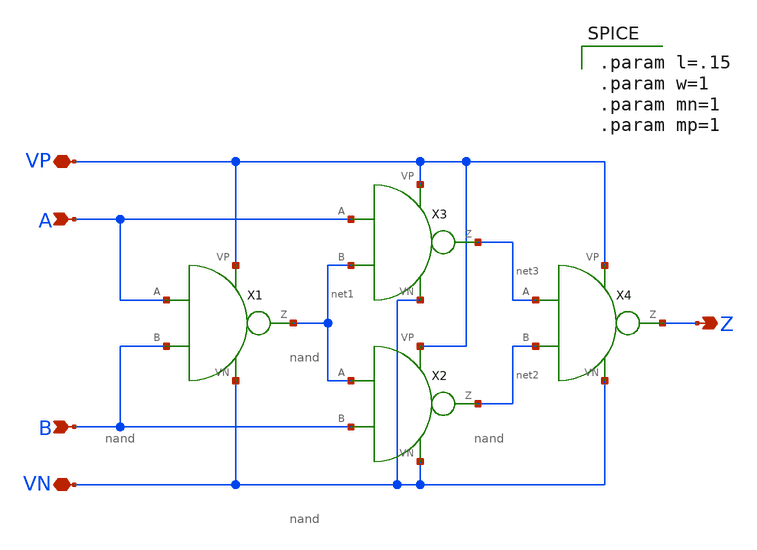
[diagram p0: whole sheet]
** sch_path: schematics/xor.sch
**.subckt xor A B VP VN Z
*.ipin A
*.ipin B
*.iopin VP
*.iopin VN
*.opin Z
X1 A B VP VN net1 nand
X2 net1 B VP VN net2 nand
X3 A net1 VP VN net3 nand
X4 net3 net2 VP VN Z nand
**** begin user architecture code

.param l=.15
.param w=1
.param mn=1
.param mp=1

**** end user architecture code
**.ends

* expanding   symbol:  /home/madvlsi/Documents/MADVLSI_final/schematics/nand.sym # of pins=6
** sym_path: schematics/nand.sym
** sch_path: schematics/nand.sch
.subckt nand A B VP VN Z
*.ipin A
*.iopin VP
*.iopin VN
*.opin Z
*.ipin B
XM1 Z A net1 GND sky130_fd_pr__nfet_01v8 L=0.15 W=1 nf=1 ad='int((nf+1)/2) * W/nf * 0.29' as='int((nf+2)/2) * W/nf * 0.29'
+ pd='2*int((nf+1)/2) * (W/nf + 0.29)' ps='2*int((nf+2)/2) * (W/nf + 0.29)' nrd='0.29 / W' nrs='0.29 / W'
+ sa=0 sb=0 sd=0 mult=1 m=1
XM2 VP B Z VDD sky130_fd_pr__pfet_01v8 L=0.15 W=1 nf=1 ad='int((nf+1)/2) * W/nf * 0.29' as='int((nf+2)/2) * W/nf * 0.29'
+ pd='2*int((nf+1)/2) * (W/nf + 0.29)' ps='2*int((nf+2)/2) * (W/nf + 0.29)' nrd='0.29 / W' nrs='0.29 / W'
+ sa=0 sb=0 sd=0 mult=2 m=2
XM3 VN B net1 GND sky130_fd_pr__nfet_01v8 L=0.15 W=1 nf=1 ad='int((nf+1)/2) * W/nf * 0.29' as='int((nf+2)/2) * W/nf * 0.29'
+ pd='2*int((nf+1)/2) * (W/nf + 0.29)' ps='2*int((nf+2)/2) * (W/nf + 0.29)' nrd='0.29 / W' nrs='0.29 / W'
+ sa=0 sb=0 sd=0 mult=1 m=1
XM4 Z A VP VDD sky130_fd_pr__pfet_01v8 L=0.15 W=1 nf=1 ad='int((nf+1)/2) * W/nf * 0.29' as='int((nf+2)/2) * W/nf * 0.29'
+ pd='2*int((nf+1)/2) * (W/nf + 0.29)' ps='2*int((nf+2)/2) * (W/nf + 0.29)' nrd='0.29 / W' nrs='0.29 / W'
+ sa=0 sb=0 sd=0 mult=2 m=2
.ends

.end
